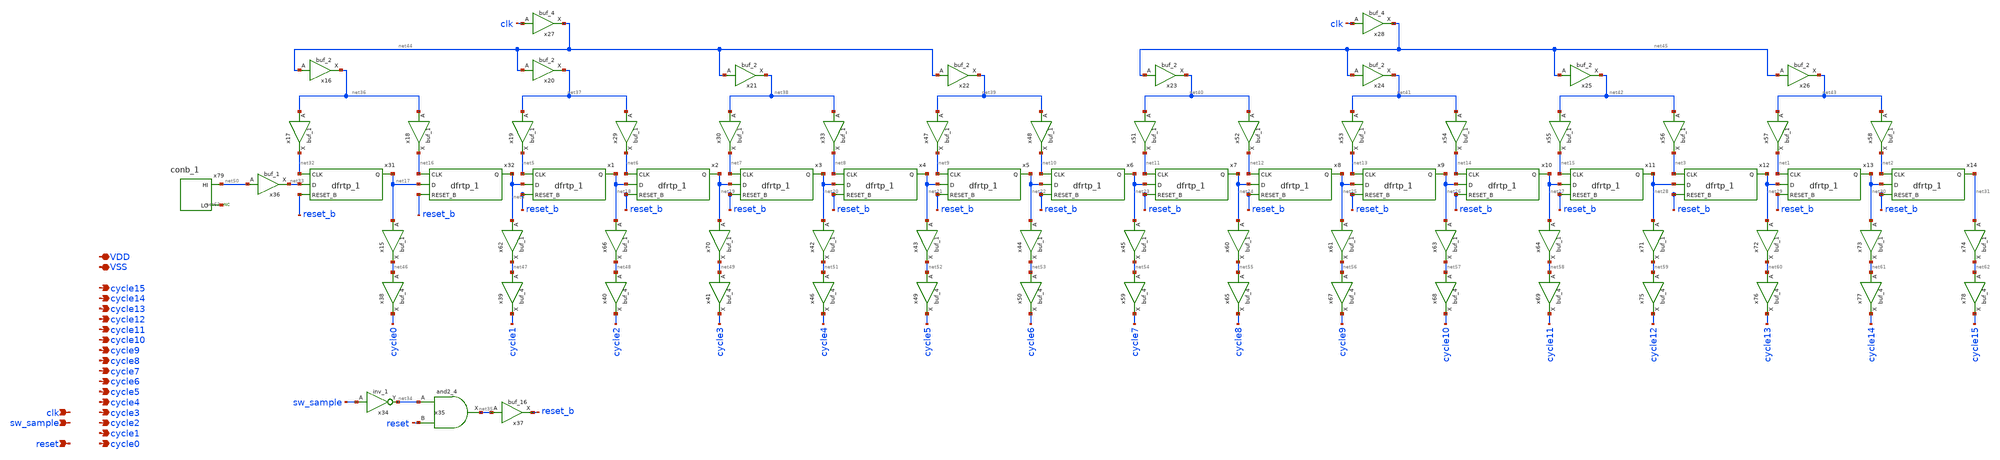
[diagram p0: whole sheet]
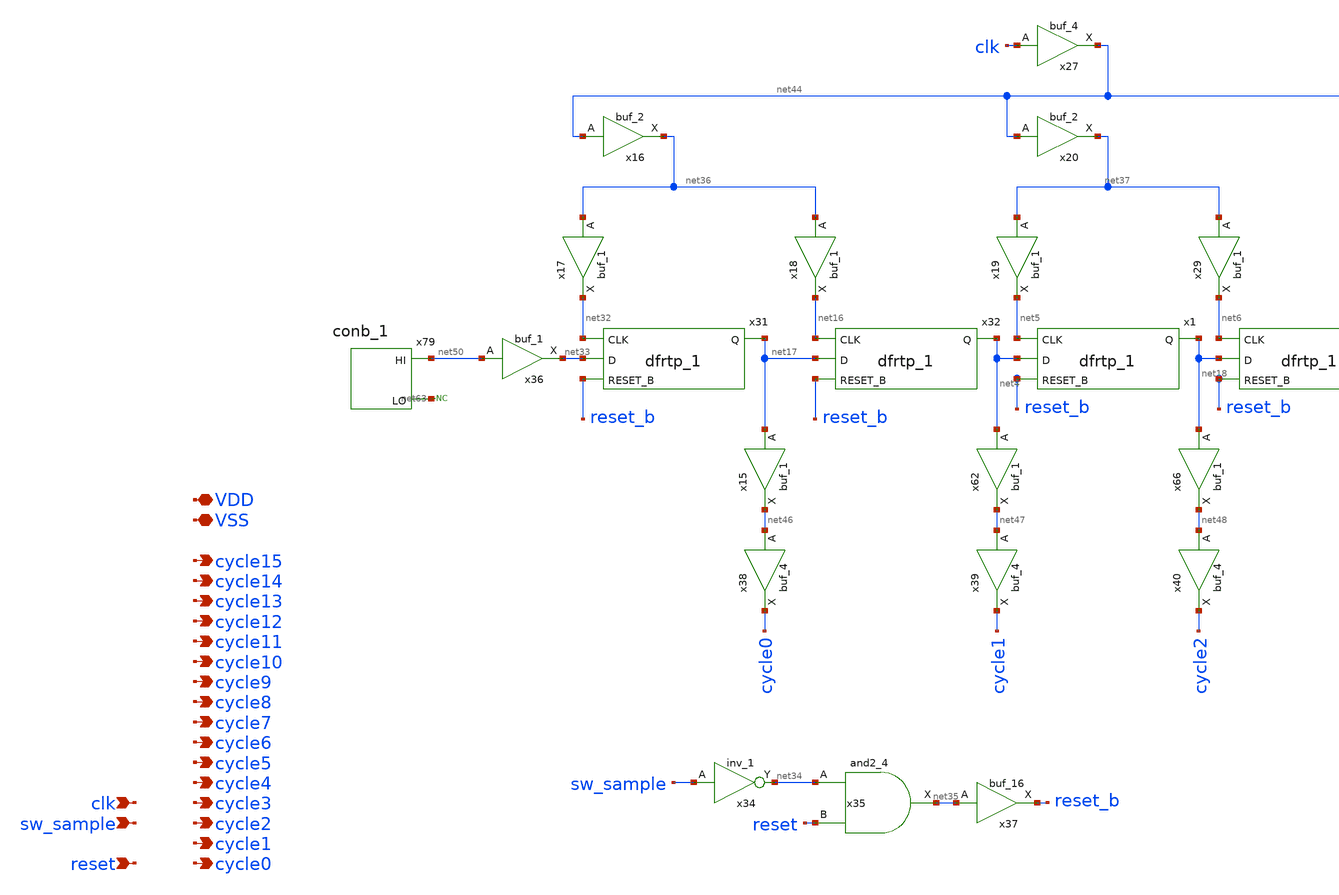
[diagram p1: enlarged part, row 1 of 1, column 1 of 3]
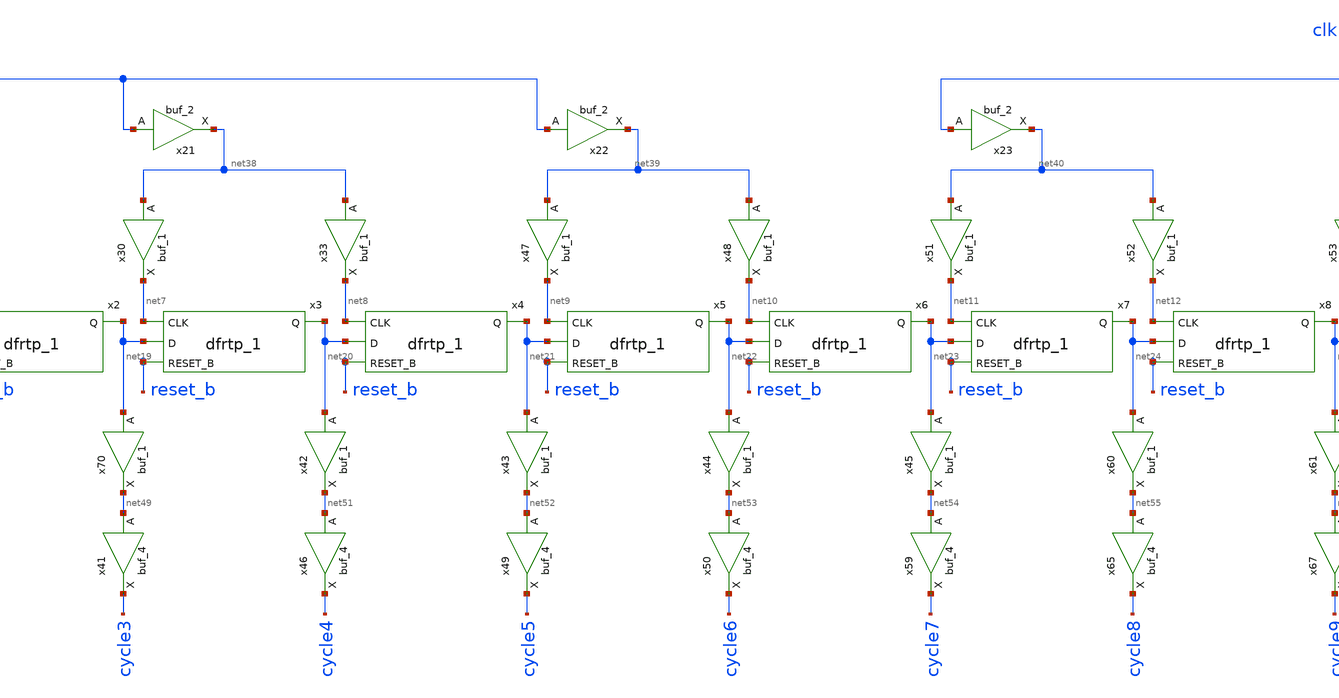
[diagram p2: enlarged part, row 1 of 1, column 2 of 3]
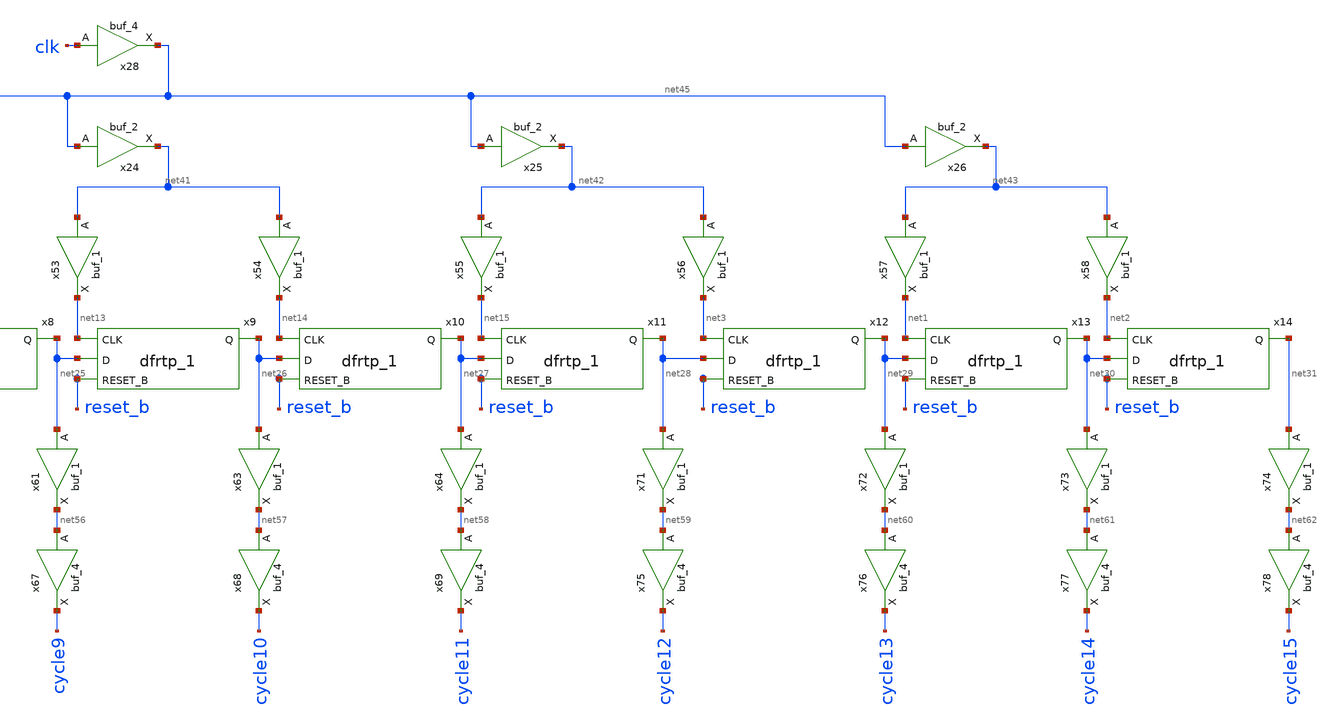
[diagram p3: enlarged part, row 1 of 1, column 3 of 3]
** sch_path: xschem/src/shifted_clock_generator/shifted_clock_generator.sch
**.subckt shifted_clock_generator cycle15 VSS VDD clk reset sw_sample cycle14 cycle13 cycle12
*+ cycle11 cycle10 cycle9 cycle8 cycle7 cycle6 cycle5 cycle4 cycle3 cycle2 cycle1 cycle0
*.opin cycle15
*.iopin VSS
*.iopin VDD
*.ipin clk
*.ipin reset
*.ipin sw_sample
*.opin cycle14
*.opin cycle13
*.opin cycle12
*.opin cycle11
*.opin cycle10
*.opin cycle9
*.opin cycle8
*.opin cycle7
*.opin cycle6
*.opin cycle5
*.opin cycle4
*.opin cycle3
*.opin cycle2
*.opin cycle1
*.opin cycle0
x32 net16 net17 reset_b VSS VSS VDD VDD net4 sky130_fd_sc_hd__dfrtp_1
x1 net5 net4 reset_b VSS VSS VDD VDD net18 sky130_fd_sc_hd__dfrtp_1
x2 net6 net18 reset_b VSS VSS VDD VDD net19 sky130_fd_sc_hd__dfrtp_1
x3 net7 net19 reset_b VSS VSS VDD VDD net20 sky130_fd_sc_hd__dfrtp_1
x4 net8 net20 reset_b VSS VSS VDD VDD net21 sky130_fd_sc_hd__dfrtp_1
x5 net9 net21 reset_b VSS VSS VDD VDD net22 sky130_fd_sc_hd__dfrtp_1
x6 net10 net22 reset_b VSS VSS VDD VDD net23 sky130_fd_sc_hd__dfrtp_1
x7 net11 net23 reset_b VSS VSS VDD VDD net24 sky130_fd_sc_hd__dfrtp_1
x8 net12 net24 reset_b VSS VSS VDD VDD net25 sky130_fd_sc_hd__dfrtp_1
x9 net13 net25 reset_b VSS VSS VDD VDD net26 sky130_fd_sc_hd__dfrtp_1
x10 net14 net26 reset_b VSS VSS VDD VDD net27 sky130_fd_sc_hd__dfrtp_1
x11 net15 net27 reset_b VSS VSS VDD VDD net28 sky130_fd_sc_hd__dfrtp_1
x12 net3 net28 reset_b VSS VSS VDD VDD net29 sky130_fd_sc_hd__dfrtp_1
x13 net1 net29 reset_b VSS VSS VDD VDD net30 sky130_fd_sc_hd__dfrtp_1
x14 net2 net30 reset_b VSS VSS VDD VDD net31 sky130_fd_sc_hd__dfrtp_1
x31 net32 net33 reset_b VSS VSS VDD VDD net17 sky130_fd_sc_hd__dfrtp_1
x37 net35 VSS VSS VDD VDD reset_b sky130_fd_sc_hd__buf_16
x35 net34 reset VSS VSS VDD VDD net35 sky130_fd_sc_hd__and2_4
x15 net17 VSS VSS VDD VDD net46 sky130_fd_sc_hd__buf_1
x16 net44 VSS VSS VDD VDD net36 sky130_fd_sc_hd__buf_2
x20 net44 VSS VSS VDD VDD net37 sky130_fd_sc_hd__buf_2
x21 net44 VSS VSS VDD VDD net38 sky130_fd_sc_hd__buf_2
x22 net44 VSS VSS VDD VDD net39 sky130_fd_sc_hd__buf_2
x23 net45 VSS VSS VDD VDD net40 sky130_fd_sc_hd__buf_2
x24 net45 VSS VSS VDD VDD net41 sky130_fd_sc_hd__buf_2
x25 net45 VSS VSS VDD VDD net42 sky130_fd_sc_hd__buf_2
x26 net45 VSS VSS VDD VDD net43 sky130_fd_sc_hd__buf_2
x27 clk VSS VSS VDD VDD net44 sky130_fd_sc_hd__buf_4
x28 clk VSS VSS VDD VDD net45 sky130_fd_sc_hd__buf_4
x17 net36 VSS VSS VDD VDD net32 sky130_fd_sc_hd__buf_1
x18 net36 VSS VSS VDD VDD net16 sky130_fd_sc_hd__buf_1
x19 net37 VSS VSS VDD VDD net5 sky130_fd_sc_hd__buf_1
x29 net37 VSS VSS VDD VDD net6 sky130_fd_sc_hd__buf_1
x30 net38 VSS VSS VDD VDD net7 sky130_fd_sc_hd__buf_1
x33 net38 VSS VSS VDD VDD net8 sky130_fd_sc_hd__buf_1
x47 net39 VSS VSS VDD VDD net9 sky130_fd_sc_hd__buf_1
x48 net39 VSS VSS VDD VDD net10 sky130_fd_sc_hd__buf_1
x51 net40 VSS VSS VDD VDD net11 sky130_fd_sc_hd__buf_1
x52 net40 VSS VSS VDD VDD net12 sky130_fd_sc_hd__buf_1
x53 net41 VSS VSS VDD VDD net13 sky130_fd_sc_hd__buf_1
x54 net41 VSS VSS VDD VDD net14 sky130_fd_sc_hd__buf_1
x55 net42 VSS VSS VDD VDD net15 sky130_fd_sc_hd__buf_1
x56 net42 VSS VSS VDD VDD net3 sky130_fd_sc_hd__buf_1
x57 net43 VSS VSS VDD VDD net1 sky130_fd_sc_hd__buf_1
x58 net43 VSS VSS VDD VDD net2 sky130_fd_sc_hd__buf_1
x62 net4 VSS VSS VDD VDD net47 sky130_fd_sc_hd__buf_1
x66 net18 VSS VSS VDD VDD net48 sky130_fd_sc_hd__buf_1
x70 net19 VSS VSS VDD VDD net49 sky130_fd_sc_hd__buf_1
x34 sw_sample VSS VSS VDD VDD net34 sky130_fd_sc_hd__inv_1
x36 net50 VSS VSS VDD VDD net33 sky130_fd_sc_hd__buf_1
x38 net46 VSS VSS VDD VDD cycle0 sky130_fd_sc_hd__buf_4
x39 net47 VSS VSS VDD VDD cycle1 sky130_fd_sc_hd__buf_4
x40 net48 VSS VSS VDD VDD cycle2 sky130_fd_sc_hd__buf_4
x41 net49 VSS VSS VDD VDD cycle3 sky130_fd_sc_hd__buf_4
x42 net20 VSS VSS VDD VDD net51 sky130_fd_sc_hd__buf_1
x43 net21 VSS VSS VDD VDD net52 sky130_fd_sc_hd__buf_1
x44 net22 VSS VSS VDD VDD net53 sky130_fd_sc_hd__buf_1
x45 net23 VSS VSS VDD VDD net54 sky130_fd_sc_hd__buf_1
x46 net51 VSS VSS VDD VDD cycle4 sky130_fd_sc_hd__buf_4
x49 net52 VSS VSS VDD VDD cycle5 sky130_fd_sc_hd__buf_4
x50 net53 VSS VSS VDD VDD cycle6 sky130_fd_sc_hd__buf_4
x59 net54 VSS VSS VDD VDD cycle7 sky130_fd_sc_hd__buf_4
x60 net24 VSS VSS VDD VDD net55 sky130_fd_sc_hd__buf_1
x61 net25 VSS VSS VDD VDD net56 sky130_fd_sc_hd__buf_1
x63 net26 VSS VSS VDD VDD net57 sky130_fd_sc_hd__buf_1
x64 net27 VSS VSS VDD VDD net58 sky130_fd_sc_hd__buf_1
x65 net55 VSS VSS VDD VDD cycle8 sky130_fd_sc_hd__buf_4
x67 net56 VSS VSS VDD VDD cycle9 sky130_fd_sc_hd__buf_4
x68 net57 VSS VSS VDD VDD cycle10 sky130_fd_sc_hd__buf_4
x69 net58 VSS VSS VDD VDD cycle11 sky130_fd_sc_hd__buf_4
x71 net28 VSS VSS VDD VDD net59 sky130_fd_sc_hd__buf_1
x72 net29 VSS VSS VDD VDD net60 sky130_fd_sc_hd__buf_1
x73 net30 VSS VSS VDD VDD net61 sky130_fd_sc_hd__buf_1
x74 net31 VSS VSS VDD VDD net62 sky130_fd_sc_hd__buf_1
x75 net59 VSS VSS VDD VDD cycle12 sky130_fd_sc_hd__buf_4
x76 net60 VSS VSS VDD VDD cycle13 sky130_fd_sc_hd__buf_4
x77 net61 VSS VSS VDD VDD cycle14 sky130_fd_sc_hd__buf_4
x78 net62 VSS VSS VDD VDD cycle15 sky130_fd_sc_hd__buf_4
x79 VSS VSS VDD VDD net50 net63 sky130_fd_sc_hd__conb_1
* noconn #net63
**.ends
.end
